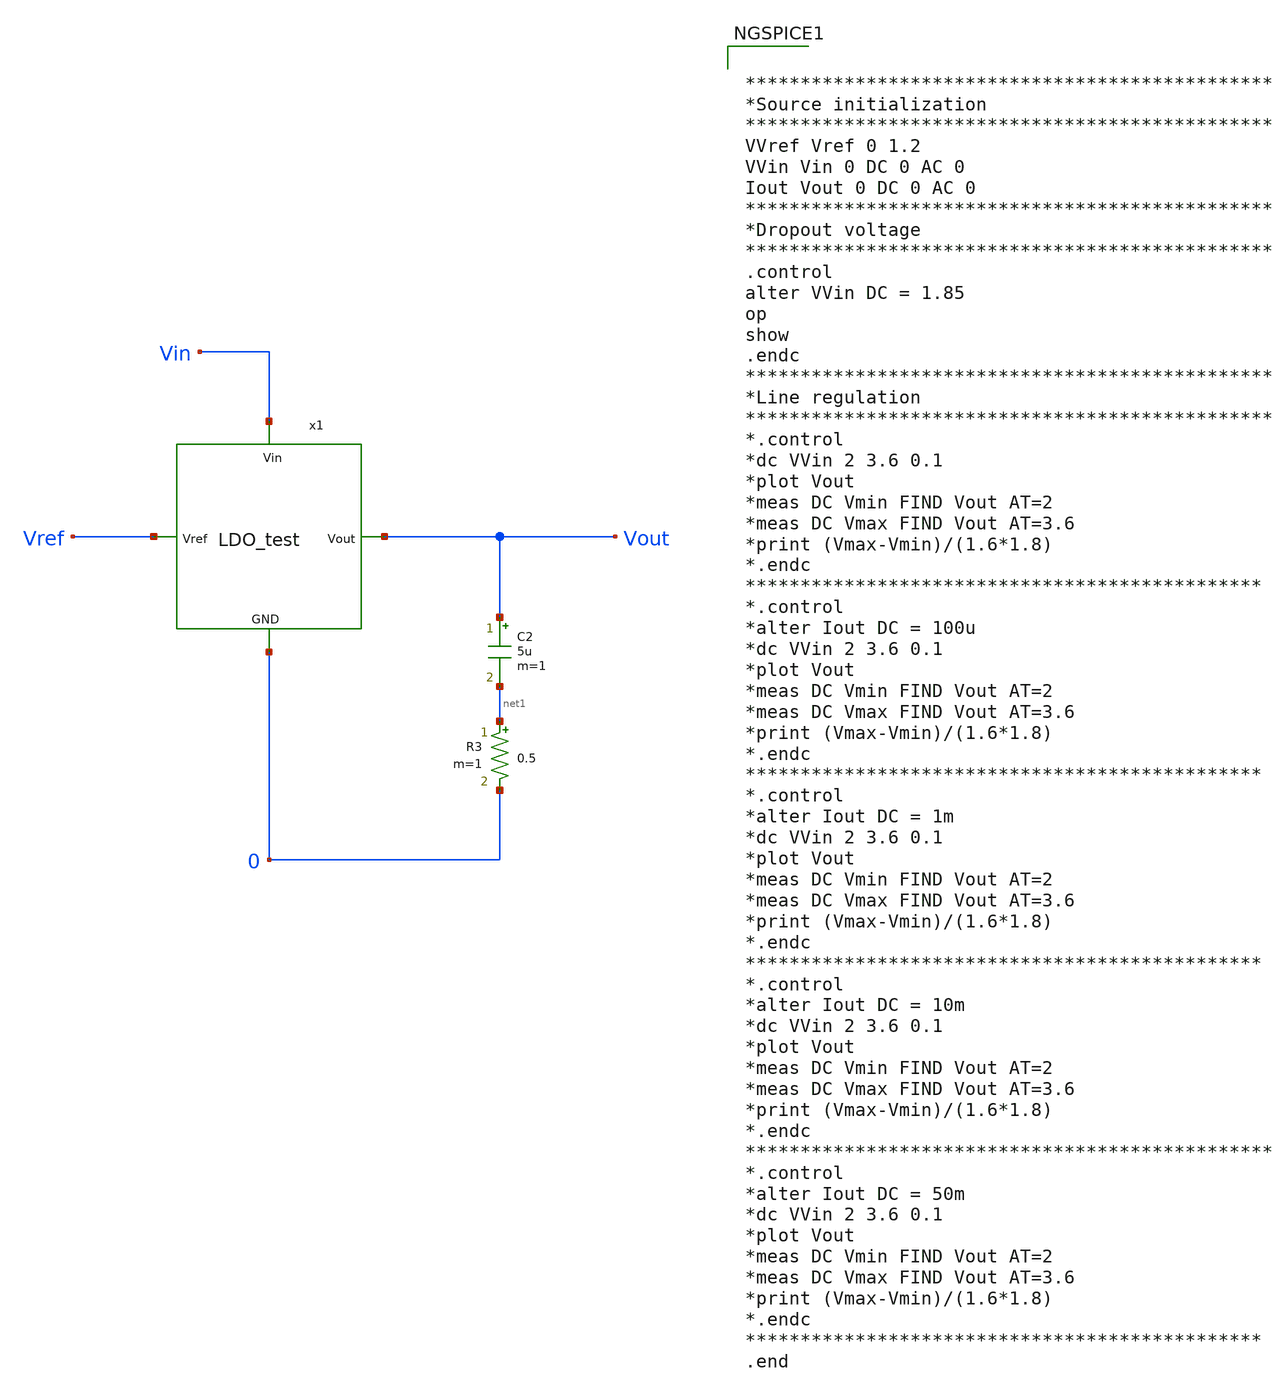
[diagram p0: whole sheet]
** sch_path: Analog_Blocks/LDO/Testbench/LDO_test_TB.sch
**.subckt LDO_test_TB
C2 Vout net1 5u m=1
R3 net1 0 0.5 m=1
x1 Vin Vref Vout 0 LDO_test
**** begin user architecture code


************************************************
*Source initialization
************************************************
VVref Vref 0 1.2
VVin Vin 0 DC 0 AC 0
Iout Vout 0 DC 0 AC 0
************************************************
*Dropout voltage
************************************************
.control
alter VVin DC = 1.85
op
show
.endc
************************************************
*Line regulation
************************************************
*.control
*dc VVin 2 3.6 0.1
*plot Vout
*meas DC Vmin FIND Vout AT=2
*meas DC Vmax FIND Vout AT=3.6
*print (Vmax-Vmin)/(1.6*1.8)
*.endc
***********************************************
*.control
*alter Iout DC = 100u
*dc VVin 2 3.6 0.1
*plot Vout
*meas DC Vmin FIND Vout AT=2
*meas DC Vmax FIND Vout AT=3.6
*print (Vmax-Vmin)/(1.6*1.8)
*.endc
***********************************************
*.control
*alter Iout DC = 1m
*dc VVin 2 3.6 0.1
*plot Vout
*meas DC Vmin FIND Vout AT=2
*meas DC Vmax FIND Vout AT=3.6
*print (Vmax-Vmin)/(1.6*1.8)
*.endc
***********************************************
*.control
*alter Iout DC = 10m
*dc VVin 2 3.6 0.1
*plot Vout
*meas DC Vmin FIND Vout AT=2
*meas DC Vmax FIND Vout AT=3.6
*print (Vmax-Vmin)/(1.6*1.8)
*.endc
************************************************
*.control
*alter Iout DC = 50m
*dc VVin 2 3.6 0.1
*plot Vout
*meas DC Vmin FIND Vout AT=2
*meas DC Vmax FIND Vout AT=3.6
*print (Vmax-Vmin)/(1.6*1.8)
*.endc
***********************************************
.end




.param mc_mm_switch=0
.param mc_pr_switch=0
.include ~/mabrains/Analog_blocks/models/sky130A/libs.ref/sky130_fd_pr/spice/sky130_fd_pr__nfet_01v8__tt.corner.spice
.include ~/mabrains/Analog_blocks/models/sky130A/libs.ref/sky130_fd_pr/spice/sky130_fd_pr__nfet_01v8_lvt__tt.corner.spice
.include ~/mabrains/Analog_blocks/models/sky130A/libs.ref/sky130_fd_pr/spice/sky130_fd_pr__pfet_01v8__tt.corner.spice
.include ~/mabrains/Analog_blocks/models/sky130A/libs.ref/sky130_fd_pr/spice/sky130_fd_pr__nfet_03v3_nvt__tt.corner.spice
.include ~/mabrains/Analog_blocks/models/sky130A/libs.ref/sky130_fd_pr/spice/sky130_fd_pr__nfet_05v0_nvt__tt.corner.spice
.include ~/mabrains/Analog_blocks/models/sky130A/libs.ref/sky130_fd_pr/spice/sky130_fd_pr__esd_nfet_01v8__tt.corner.spice
.include ~/mabrains/Analog_blocks/models/sky130A/libs.ref/sky130_fd_pr/spice/sky130_fd_pr__pfet_01v8_lvt__tt.corner.spice
.include ~/mabrains/Analog_blocks/models/sky130A/libs.ref/sky130_fd_pr/spice/sky130_fd_pr__pfet_01v8_hvt__tt.corner.spice
.include ~/mabrains/Analog_blocks/models/sky130A/libs.ref/sky130_fd_pr/spice/sky130_fd_pr__esd_pfet_g5v0d10v5__tt.corner.spice
.include ~/mabrains/Analog_blocks/models/sky130A/libs.ref/sky130_fd_pr/spice/sky130_fd_pr__pfet_g5v0d10v5__tt.corner.spice
.include ~/mabrains/Analog_blocks/models/sky130A/libs.ref/sky130_fd_pr/spice/sky130_fd_pr__pfet_g5v0d16v0__tt.corner.spice
.include ~/mabrains/Analog_blocks/models/sky130A/libs.ref/sky130_fd_pr/spice/sky130_fd_pr__nfet_g5v0d10v5__tt.corner.spice
.include ~/mabrains/Analog_blocks/models/sky130A/libs.ref/sky130_fd_pr/spice/sky130_fd_pr__nfet_g5v0d16v0__tt_discrete.corner.spice
.include ~/mabrains/Analog_blocks/models/sky130A/libs.ref/sky130_fd_pr/spice/sky130_fd_pr__esd_nfet_g5v0d10v5__tt.corner.spice
.include ~/mabrains/Analog_blocks/models/sky130A/libs.tech/ngspice/corners/tt/nonfet.spice
* Mismatch parameters
.include ~/mabrains/Analog_blocks/models/sky130A/libs.ref/sky130_fd_pr/spice/sky130_fd_pr__nfet_01v8__mismatch.corner.spice
.include ~/mabrains/Analog_blocks/models/sky130A/libs.ref/sky130_fd_pr/spice/sky130_fd_pr__pfet_01v8__mismatch.corner.spice
.include ~/mabrains/Analog_blocks/models/sky130A/libs.ref/sky130_fd_pr/spice/sky130_fd_pr__nfet_01v8_lvt__mismatch.corner.spice
.include ~/mabrains/Analog_blocks/models/sky130A/libs.ref/sky130_fd_pr/spice/sky130_fd_pr__pfet_01v8_lvt__mismatch.corner.spice
.include ~/mabrains/Analog_blocks/models/sky130A/libs.ref/sky130_fd_pr/spice/sky130_fd_pr__pfet_01v8_hvt__mismatch.corner.spice
.include ~/mabrains/Analog_blocks/models/sky130A/libs.ref/sky130_fd_pr/spice/sky130_fd_pr__nfet_g5v0d10v5__mismatch.corner.spice
.include ~/mabrains/Analog_blocks/models/sky130A/libs.ref/sky130_fd_pr/spice/sky130_fd_pr__pfet_g5v0d10v5__mismatch.corner.spice
.include ~/mabrains/Analog_blocks/models/sky130A/libs.ref/sky130_fd_pr/spice/sky130_fd_pr__nfet_05v0_nvt__mismatch.corner.spice
.include ~/mabrains/Analog_blocks/models/sky130A/libs.ref/sky130_fd_pr/spice/sky130_fd_pr__nfet_03v3_nvt__mismatch.corner.spice
* Resistor/Capacitor
.include ~/mabrains/Analog_blocks/models/sky130A/libs.tech/ngspice/r+c/res_typical__cap_typical.spice
.include ~/mabrains/Analog_blocks/models/sky130A/libs.tech/ngspice/r+c/res_typical__cap_typical__lin.spice
* Special cells
.include ~/mabrains/Analog_blocks/models/sky130A/libs.tech/ngspice/corners/tt/specialized_cells.spice
* All models
.include ~/mabrains/Analog_blocks/models/sky130A/libs.tech/ngspice/all.spice
* Corner
.include ~/mabrains/Analog_blocks/models/sky130A/libs.tech/ngspice/corners/tt/rf.spice



**** end user architecture code
**.ends
.end
